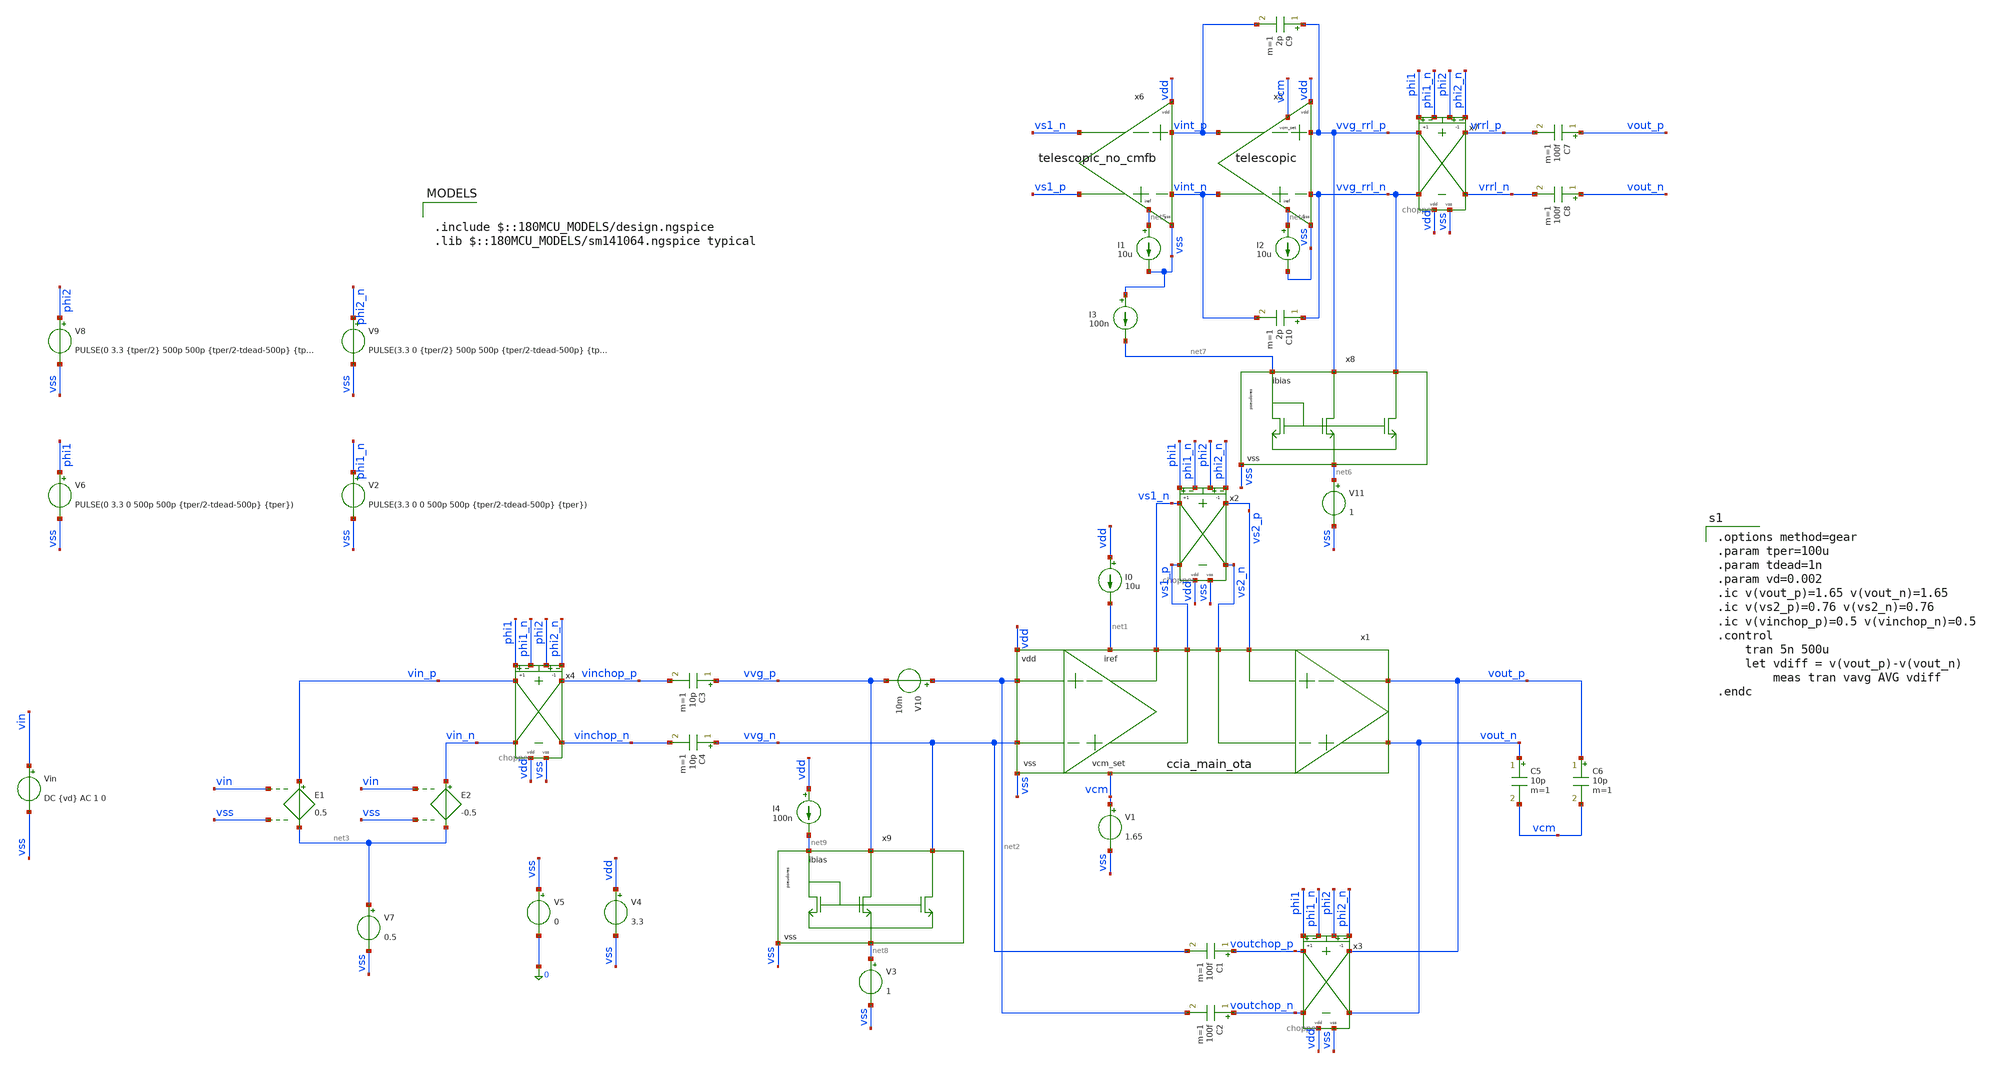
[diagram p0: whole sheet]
** sch_path: xschem/archive/ccia_top_level/ccia_top_level.sch
**.subckt ccia_top_level
x1 net2 vdd vs1_p net1 vvg_n vss vs1_n vs2_p vcm vout_n vs2_n vout_p ccia_main_ota
x2 phi1 vss vs1_n phi2 vs1_p phi1_n phi2_n vs2_p vs2_n vdd chopper
I0 vdd net1 10u
V1 vcm vss 1.65
C1 voutchop_p vvg_n 100f m=1
C2 voutchop_n net2 100f m=1
x3 phi1 vss voutchop_p phi2 voutchop_n phi1_n phi2_n vout_p vout_n vdd chopper
x4 phi1 vss vin_p phi2 vin_n phi1_n phi2_n vinchop_p vinchop_n vdd chopper
C3 vvg_p vinchop_p 10p m=1
C4 vvg_n vinchop_n 10p m=1
C5 vout_n vcm 10p m=1
C6 vout_p vcm 10p m=1
E1 vin_p net3 vin vss 0.5
E2 vin_n net3 vin vss -0.5
Vin vin vss DC {vd} AC 1 0
V6 phi1 vss PULSE(0 3.3 0 500p 500p {tper/2-tdead-500p} {tper})
V2 phi1_n vss PULSE(3.3 0 0 500p 500p {tper/2-tdead-500p} {tper})
V8 phi2 vss PULSE(0 3.3 {tper/2} 500p 500p {tper/2-tdead-500p} {tper})
V9 phi2_n vss PULSE(3.3 0 {tper/2} 500p 500p {tper/2-tdead-500p} {tper})
V4 vdd vss 3.3
V5 vss 0 0
V7 net3 vss 0.5
V10 net2 vvg_p 10m
x5 vvg_rrl_p vvg_rrl_n vint_n vint_p vdd vss vcm net4 telescopic
C7 vout_p vrrl_p 100f m=1
C8 vout_n vrrl_n 100f m=1
x7 phi1 vss vvg_rrl_p phi2 vvg_rrl_n phi1_n phi2_n vrrl_p vrrl_n vdd chopper
C9 vvg_rrl_p vint_p 2p m=1
C10 vvg_rrl_n vint_n 2p m=1
x6 vint_p vint_n vs1_p vs1_n vdd vss net5 telescopic_no_cmfb
I1 net5 vss 10u
I2 net4 vss 10u
V11 net6 vss 1
x8 net7 vvg_rrl_p vvg_rrl_n net6 vss pseudores
I3 vss net7 100n
V3 net8 vss 1
x9 net9 vvg_p vvg_n net8 vss pseudores
I4 vdd net9 100n
**** begin user architecture code

.options method=gear
.param tper=100u
.param tdead=1n
.param vd=0.002
.ic v(vout_p)=1.65 v(vout_n)=1.65
.ic v(vs2_p)=0.76 v(vs2_n)=0.76
.ic v(vinchop_p)=0.5 v(vinchop_n)=0.5
.control
	tran 5n 500u
	let vdiff = v(vout_p)-v(vout_n)
        meas tran vavg AVG vdiff
.endc


.include $::180MCU_MODELS/design.ngspice
.lib $::180MCU_MODELS/sm141064.ngspice typical

**** end user architecture code
**.ends
.end
